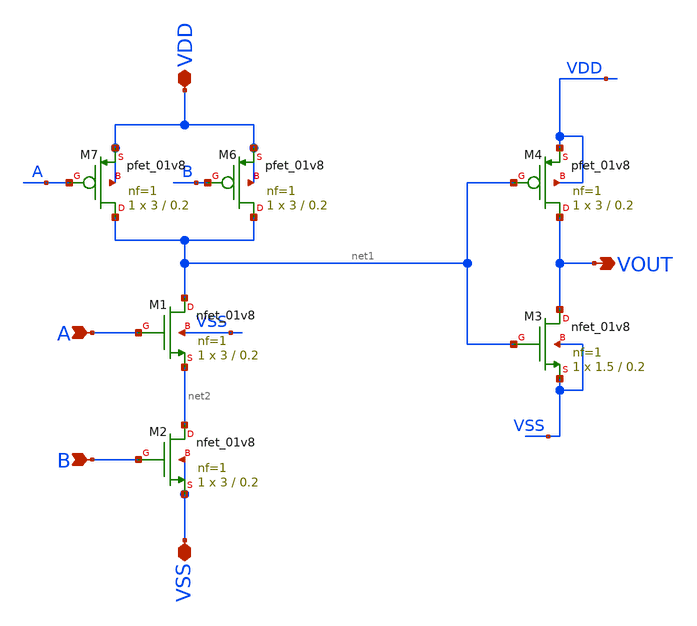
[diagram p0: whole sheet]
** sch_path: Xschem/DIVIDER/AND.sch
**.subckt AND VDD VSS A B VOUT
*.iopin VDD
*.iopin VSS
*.ipin A
*.ipin B
*.opin VOUT
XM1 net1 A net2 VSS sky130_fd_pr__nfet_01v8 L=0.2 W=3 nf=1 ad='int((nf+1)/2) * W/nf * 0.29' as='int((nf+2)/2) * W/nf * 0.29'
+ pd='2*int((nf+1)/2) * (W/nf + 0.29)' ps='2*int((nf+2)/2) * (W/nf + 0.29)' nrd='0.29 / W' nrs='0.29 / W'
+ sa=0 sb=0 sd=0 mult=1 m=1
XM2 net2 B VSS VSS sky130_fd_pr__nfet_01v8 L=0.2 W=3 nf=1 ad='int((nf+1)/2) * W/nf * 0.29' as='int((nf+2)/2) * W/nf * 0.29'
+ pd='2*int((nf+1)/2) * (W/nf + 0.29)' ps='2*int((nf+2)/2) * (W/nf + 0.29)' nrd='0.29 / W' nrs='0.29 / W'
+ sa=0 sb=0 sd=0 mult=1 m=1
XM3 VOUT net1 VSS VSS sky130_fd_pr__nfet_01v8 L=0.2 W=1.5 nf=1 ad='int((nf+1)/2) * W/nf * 0.29' as='int((nf+2)/2) * W/nf * 0.29'
+ pd='2*int((nf+1)/2) * (W/nf + 0.29)' ps='2*int((nf+2)/2) * (W/nf + 0.29)' nrd='0.29 / W' nrs='0.29 / W'
+ sa=0 sb=0 sd=0 mult=1 m=1
XM4 VOUT net1 VDD VDD sky130_fd_pr__pfet_01v8 L=0.2 W=3 nf=1 ad='int((nf+1)/2) * W/nf * 0.29' as='int((nf+2)/2) * W/nf * 0.29'
+ pd='2*int((nf+1)/2) * (W/nf + 0.29)' ps='2*int((nf+2)/2) * (W/nf + 0.29)' nrd='0.29 / W' nrs='0.29 / W'
+ sa=0 sb=0 sd=0 mult=1 m=1
XM6 net1 B VDD VDD sky130_fd_pr__pfet_01v8 L=0.2 W=3 nf=1 ad='int((nf+1)/2) * W/nf * 0.29' as='int((nf+2)/2) * W/nf * 0.29'
+ pd='2*int((nf+1)/2) * (W/nf + 0.29)' ps='2*int((nf+2)/2) * (W/nf + 0.29)' nrd='0.29 / W' nrs='0.29 / W'
+ sa=0 sb=0 sd=0 mult=1 m=1
XM7 net1 A VDD VDD sky130_fd_pr__pfet_01v8 L=0.2 W=3 nf=1 ad='int((nf+1)/2) * W/nf * 0.29' as='int((nf+2)/2) * W/nf * 0.29'
+ pd='2*int((nf+1)/2) * (W/nf + 0.29)' ps='2*int((nf+2)/2) * (W/nf + 0.29)' nrd='0.29 / W' nrs='0.29 / W'
+ sa=0 sb=0 sd=0 mult=1 m=1
**.ends
.end
